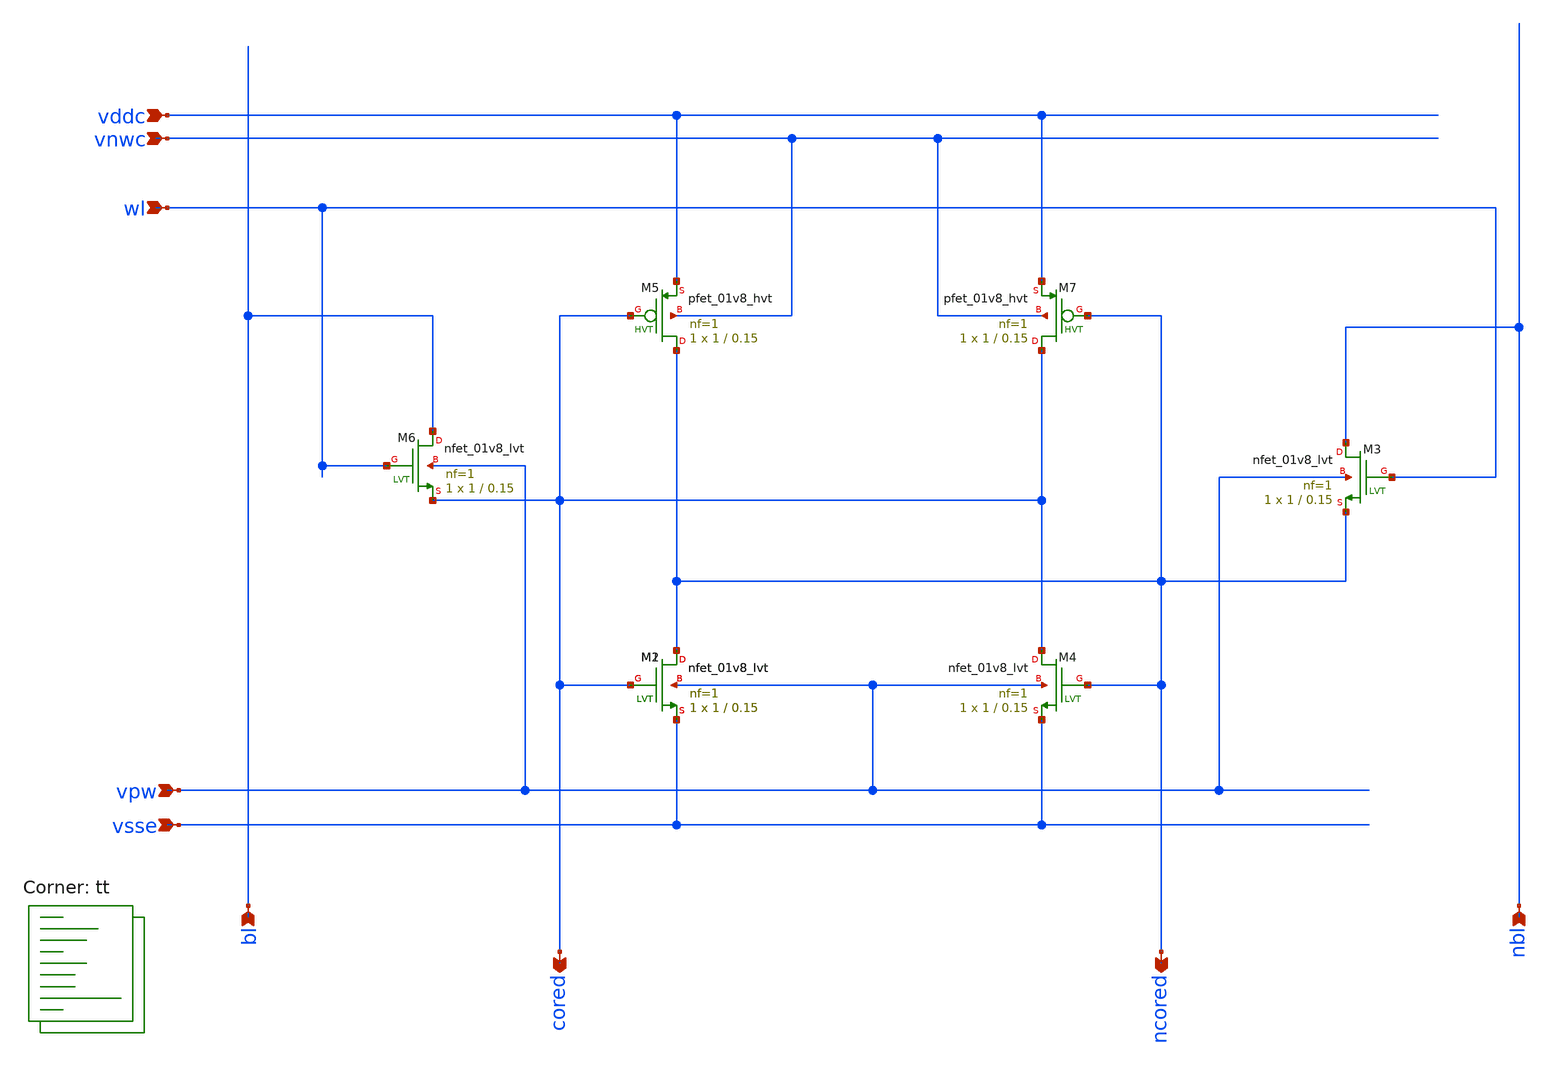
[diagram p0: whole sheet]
** sch_path: xscheme/6t.sch
**.subckt 6t vddc vpw vsse vnwc wl bl nbl cored ncored
*.ipin vddc
*.ipin vpw
*.ipin vsse
*.ipin vnwc
*.ipin wl
*.ipin bl
*.ipin nbl
*.opin cored
*.opin ncored
XM1 ncored cored vsse vpw sky130_fd_pr__nfet_01v8_lvt L=0.15 W=1 nf=1 ad='int((nf+1)/2) * W/nf * 0.29'
+ as='int((nf+2)/2) * W/nf * 0.29' pd='2*int((nf+1)/2) * (W/nf + 0.29)' ps='2*int((nf+2)/2) * (W/nf + 0.29)'
+ nrd='0.29 / W' nrs='0.29 / W' sa=0 sb=0 sd=0 mult=1 m=1
XM2 ncored cored vsse vpw sky130_fd_pr__nfet_01v8_lvt L=0.15 W=1 nf=1 ad='int((nf+1)/2) * W/nf * 0.29'
+ as='int((nf+2)/2) * W/nf * 0.29' pd='2*int((nf+1)/2) * (W/nf + 0.29)' ps='2*int((nf+2)/2) * (W/nf + 0.29)'
+ nrd='0.29 / W' nrs='0.29 / W' sa=0 sb=0 sd=0 mult=1 m=1
XM6 bl wl cored vpw sky130_fd_pr__nfet_01v8_lvt L=0.15 W=1 nf=1 ad='int((nf+1)/2) * W/nf * 0.29' as='int((nf+2)/2) * W/nf * 0.29'
+ pd='2*int((nf+1)/2) * (W/nf + 0.29)' ps='2*int((nf+2)/2) * (W/nf + 0.29)' nrd='0.29 / W' nrs='0.29 / W'
+ sa=0 sb=0 sd=0 mult=1 m=1
XM4 cored ncored vsse vpw sky130_fd_pr__nfet_01v8_lvt L=0.15 W=1 nf=1 ad='int((nf+1)/2) * W/nf * 0.29'
+ as='int((nf+2)/2) * W/nf * 0.29' pd='2*int((nf+1)/2) * (W/nf + 0.29)' ps='2*int((nf+2)/2) * (W/nf + 0.29)'
+ nrd='0.29 / W' nrs='0.29 / W' sa=0 sb=0 sd=0 mult=1 m=1
XM3 nbl wl ncored vpw sky130_fd_pr__nfet_01v8_lvt L=0.15 W=1 nf=1 ad='int((nf+1)/2) * W/nf * 0.29' as='int((nf+2)/2) * W/nf * 0.29'
+ pd='2*int((nf+1)/2) * (W/nf + 0.29)' ps='2*int((nf+2)/2) * (W/nf + 0.29)' nrd='0.29 / W' nrs='0.29 / W'
+ sa=0 sb=0 sd=0 mult=1 m=1
XM5 ncored cored vddc vnwc sky130_fd_pr__pfet_01v8_hvt L=0.15 W=1 nf=1 ad='int((nf+1)/2) * W/nf * 0.29'
+ as='int((nf+2)/2) * W/nf * 0.29' pd='2*int((nf+1)/2) * (W/nf + 0.29)' ps='2*int((nf+2)/2) * (W/nf + 0.29)'
+ nrd='0.29 / W' nrs='0.29 / W' sa=0 sb=0 sd=0 mult=1 m=1
XM7 cored ncored vddc vnwc sky130_fd_pr__pfet_01v8_hvt L=0.15 W=1 nf=1 ad='int((nf+1)/2) * W/nf * 0.29'
+ as='int((nf+2)/2) * W/nf * 0.29' pd='2*int((nf+1)/2) * (W/nf + 0.29)' ps='2*int((nf+2)/2) * (W/nf + 0.29)'
+ nrd='0.29 / W' nrs='0.29 / W' sa=0 sb=0 sd=0 mult=1 m=1
**** begin user architecture code
.lib $::SKYWATER_MODELS/sky130.lib.spice tt


.OP
.TRAN 1ps 148ps
.OPTIONS POST

.save all


**** end user architecture code
**.ends
.end
